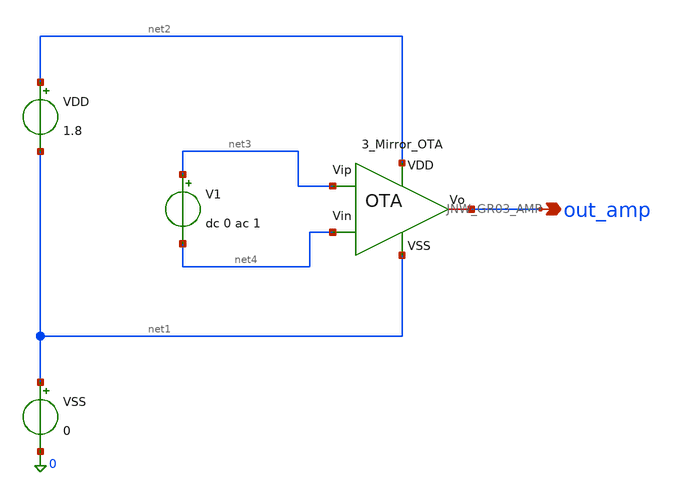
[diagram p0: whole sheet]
** sch_path: design/JNW_GR03_SKY130A/TB_JNW_GR03_AMP.sch
**.subckt TB_JNW_GR03_AMP out_amp
*.opin out_amp
x1 net2 out_amp net3 net4 net1 JNW_GR03_AMP
VDD net2 net1 1.8
VSS net1 0 0
V1 net3 net4 dc 0 ac 1
**.ends
.end
